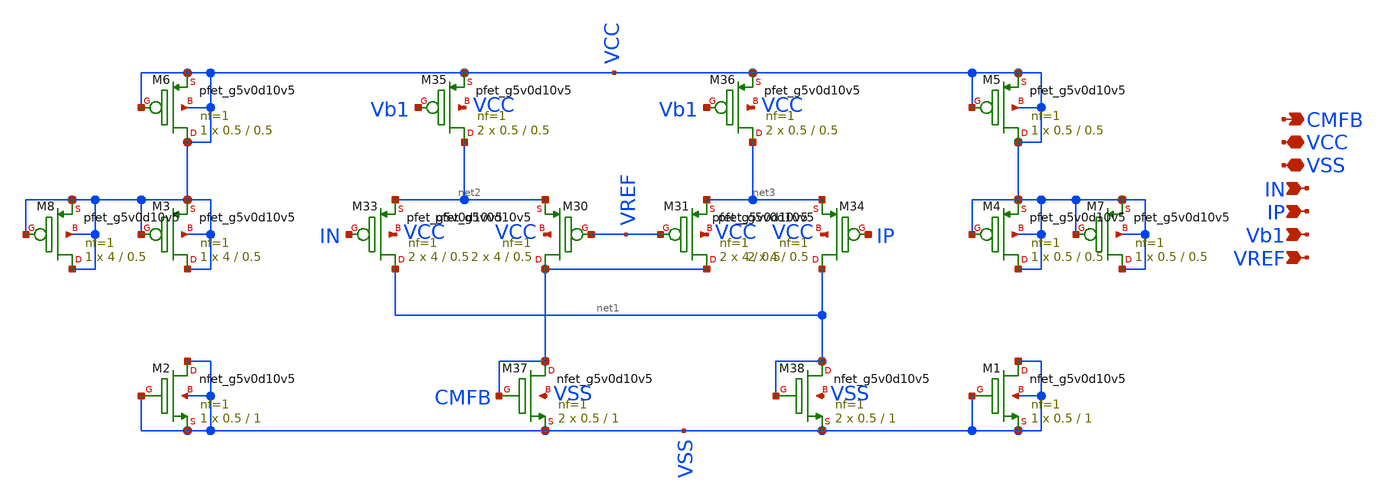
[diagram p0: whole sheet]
** sch_path: latest_working_comparator/CMFB_block.sch
**.subckt CMFB_block CMFB VCC VSS IN IP Vb1 VREF
*.opin CMFB
*.iopin VCC
*.iopin VSS
*.ipin IN
*.ipin IP
*.ipin Vb1
*.ipin VREF
XM30 CMFB VREF net2 VCC sky130_fd_pr__pfet_g5v0d10v5 L=0.5 W=4 nf=1 ad='int((nf+1)/2) * W/nf * 0.29'
+ as='int((nf+2)/2) * W/nf * 0.29' pd='2*int((nf+1)/2) * (W/nf + 0.29)' ps='2*int((nf+2)/2) * (W/nf + 0.29)'
+ nrd='0.29 / W' nrs='0.29 / W' sa=0 sb=0 sd=0 mult=2 m=2
XM31 CMFB VREF net3 VCC sky130_fd_pr__pfet_g5v0d10v5 L=0.5 W=4 nf=1 ad='int((nf+1)/2) * W/nf * 0.29'
+ as='int((nf+2)/2) * W/nf * 0.29' pd='2*int((nf+1)/2) * (W/nf + 0.29)' ps='2*int((nf+2)/2) * (W/nf + 0.29)'
+ nrd='0.29 / W' nrs='0.29 / W' sa=0 sb=0 sd=0 mult=2 m=2
XM33 net1 IN net2 VCC sky130_fd_pr__pfet_g5v0d10v5 L=0.5 W=4 nf=1 ad='int((nf+1)/2) * W/nf * 0.29' as='int((nf+2)/2) * W/nf * 0.29'
+ pd='2*int((nf+1)/2) * (W/nf + 0.29)' ps='2*int((nf+2)/2) * (W/nf + 0.29)' nrd='0.29 / W' nrs='0.29 / W'
+ sa=0 sb=0 sd=0 mult=2 m=2
XM34 net1 IP net3 VCC sky130_fd_pr__pfet_g5v0d10v5 L=0.5 W=4 nf=1 ad='int((nf+1)/2) * W/nf * 0.29' as='int((nf+2)/2) * W/nf * 0.29'
+ pd='2*int((nf+1)/2) * (W/nf + 0.29)' ps='2*int((nf+2)/2) * (W/nf + 0.29)' nrd='0.29 / W' nrs='0.29 / W'
+ sa=0 sb=0 sd=0 mult=2 m=2
XM35 net2 Vb1 VCC VCC sky130_fd_pr__pfet_g5v0d10v5 L=0.5 W=0.5 nf=1 ad='int((nf+1)/2) * W/nf * 0.29'
+ as='int((nf+2)/2) * W/nf * 0.29' pd='2*int((nf+1)/2) * (W/nf + 0.29)' ps='2*int((nf+2)/2) * (W/nf + 0.29)'
+ nrd='0.29 / W' nrs='0.29 / W' sa=0 sb=0 sd=0 mult=2 m=2
XM36 net3 Vb1 VCC VCC sky130_fd_pr__pfet_g5v0d10v5 L=0.5 W=0.5 nf=1 ad='int((nf+1)/2) * W/nf * 0.29'
+ as='int((nf+2)/2) * W/nf * 0.29' pd='2*int((nf+1)/2) * (W/nf + 0.29)' ps='2*int((nf+2)/2) * (W/nf + 0.29)'
+ nrd='0.29 / W' nrs='0.29 / W' sa=0 sb=0 sd=0 mult=2 m=2
XM37 CMFB CMFB VSS VSS sky130_fd_pr__nfet_g5v0d10v5 L=1 W=0.5 nf=1 ad='int((nf+1)/2) * W/nf * 0.29' as='int((nf+2)/2) * W/nf * 0.29'
+ pd='2*int((nf+1)/2) * (W/nf + 0.29)' ps='2*int((nf+2)/2) * (W/nf + 0.29)' nrd='0.29 / W' nrs='0.29 / W'
+ sa=0 sb=0 sd=0 mult=2 m=2
XM38 net1 net1 VSS VSS sky130_fd_pr__nfet_g5v0d10v5 L=1 W=0.5 nf=1 ad='int((nf+1)/2) * W/nf * 0.29' as='int((nf+2)/2) * W/nf * 0.29'
+ pd='2*int((nf+1)/2) * (W/nf + 0.29)' ps='2*int((nf+2)/2) * (W/nf + 0.29)' nrd='0.29 / W' nrs='0.29 / W'
+ sa=0 sb=0 sd=0 mult=2 m=2
XM1 VSS VSS VSS VSS sky130_fd_pr__nfet_g5v0d10v5 L=1 W=0.5 nf=1 ad='int((nf+1)/2) * W/nf * 0.29' as='int((nf+2)/2) * W/nf * 0.29'
+ pd='2*int((nf+1)/2) * (W/nf + 0.29)' ps='2*int((nf+2)/2) * (W/nf + 0.29)' nrd='0.29 / W' nrs='0.29 / W'
+ sa=0 sb=0 sd=0 mult=1 m=1
XM2 VSS VSS VSS VSS sky130_fd_pr__nfet_g5v0d10v5 L=1 W=0.5 nf=1 ad='int((nf+1)/2) * W/nf * 0.29' as='int((nf+2)/2) * W/nf * 0.29'
+ pd='2*int((nf+1)/2) * (W/nf + 0.29)' ps='2*int((nf+2)/2) * (W/nf + 0.29)' nrd='0.29 / W' nrs='0.29 / W'
+ sa=0 sb=0 sd=0 mult=1 m=1
XM3 VCC VCC VCC VCC sky130_fd_pr__pfet_g5v0d10v5 L=0.5 W=4 nf=1 ad='int((nf+1)/2) * W/nf * 0.29' as='int((nf+2)/2) * W/nf * 0.29'
+ pd='2*int((nf+1)/2) * (W/nf + 0.29)' ps='2*int((nf+2)/2) * (W/nf + 0.29)' nrd='0.29 / W' nrs='0.29 / W'
+ sa=0 sb=0 sd=0 mult=1 m=1
XM5 VCC VCC VCC VCC sky130_fd_pr__pfet_g5v0d10v5 L=0.5 W=0.5 nf=1 ad='int((nf+1)/2) * W/nf * 0.29' as='int((nf+2)/2) * W/nf * 0.29'
+ pd='2*int((nf+1)/2) * (W/nf + 0.29)' ps='2*int((nf+2)/2) * (W/nf + 0.29)' nrd='0.29 / W' nrs='0.29 / W'
+ sa=0 sb=0 sd=0 mult=1 m=1
XM6 VCC VCC VCC VCC sky130_fd_pr__pfet_g5v0d10v5 L=0.5 W=0.5 nf=1 ad='int((nf+1)/2) * W/nf * 0.29' as='int((nf+2)/2) * W/nf * 0.29'
+ pd='2*int((nf+1)/2) * (W/nf + 0.29)' ps='2*int((nf+2)/2) * (W/nf + 0.29)' nrd='0.29 / W' nrs='0.29 / W'
+ sa=0 sb=0 sd=0 mult=1 m=1
XM4 VCC VCC VCC VCC sky130_fd_pr__pfet_g5v0d10v5 L=0.5 W=0.5 nf=1 ad='int((nf+1)/2) * W/nf * 0.29' as='int((nf+2)/2) * W/nf * 0.29'
+ pd='2*int((nf+1)/2) * (W/nf + 0.29)' ps='2*int((nf+2)/2) * (W/nf + 0.29)' nrd='0.29 / W' nrs='0.29 / W'
+ sa=0 sb=0 sd=0 mult=1 m=1
XM7 VCC VCC VCC VCC sky130_fd_pr__pfet_g5v0d10v5 L=0.5 W=0.5 nf=1 ad='int((nf+1)/2) * W/nf * 0.29' as='int((nf+2)/2) * W/nf * 0.29'
+ pd='2*int((nf+1)/2) * (W/nf + 0.29)' ps='2*int((nf+2)/2) * (W/nf + 0.29)' nrd='0.29 / W' nrs='0.29 / W'
+ sa=0 sb=0 sd=0 mult=1 m=1
XM8 VCC VCC VCC VCC sky130_fd_pr__pfet_g5v0d10v5 L=0.5 W=4 nf=1 ad='int((nf+1)/2) * W/nf * 0.29' as='int((nf+2)/2) * W/nf * 0.29'
+ pd='2*int((nf+1)/2) * (W/nf + 0.29)' ps='2*int((nf+2)/2) * (W/nf + 0.29)' nrd='0.29 / W' nrs='0.29 / W'
+ sa=0 sb=0 sd=0 mult=1 m=1
**.ends
.end
